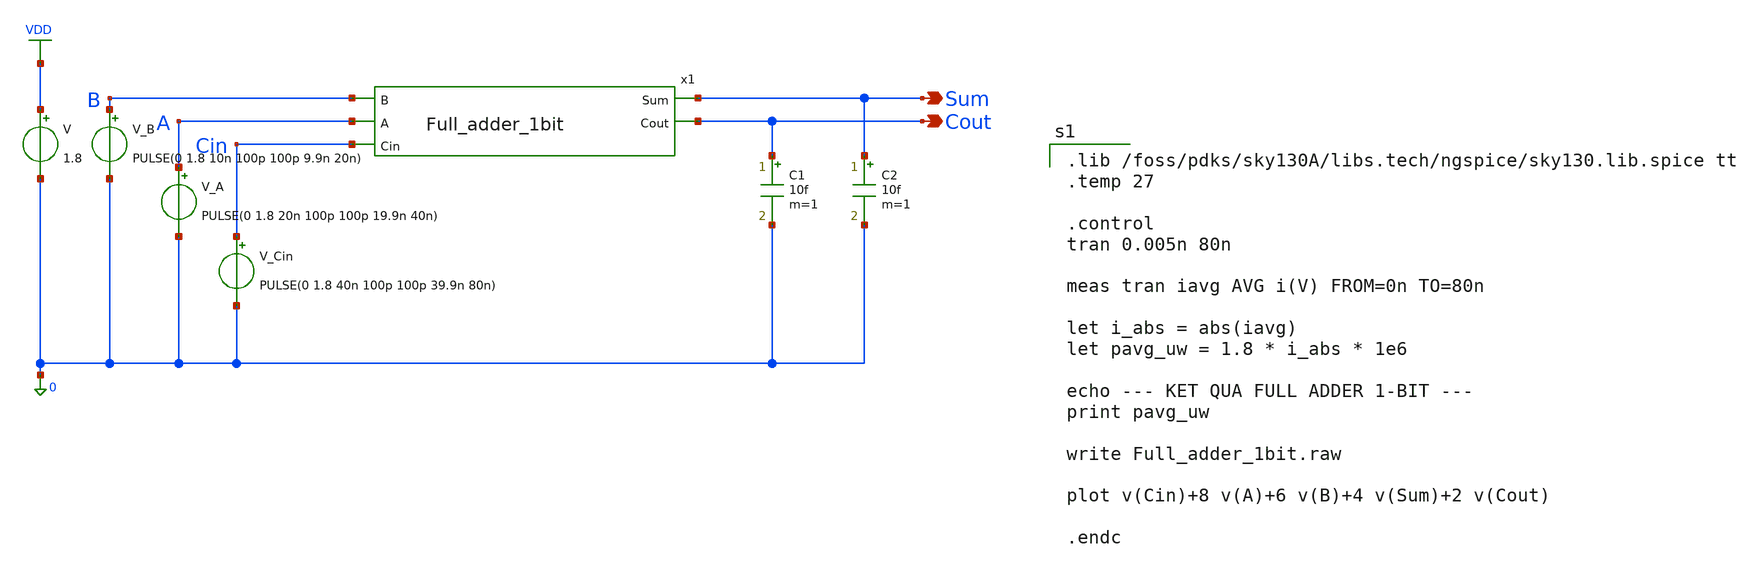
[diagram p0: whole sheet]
** sch_path: cells/full_adder_tg/xschem/tb_Full_adder_1bit.sch
**.subckt tb_Full_adder_1bit Sum Cout
*.opin Sum
*.opin Cout
x1 B A Sum Cin Cout Full_adder_1bit
V VDD 0 1.8
V_B B 0 PULSE(0 1.8 10n 100p 100p 9.9n 20n)
V_A A 0 PULSE(0 1.8 20n 100p 100p 19.9n 40n)
V_Cin Cin 0 PULSE(0 1.8 40n 100p 100p 39.9n 80n)
C1 Cout 0 10f m=1
C2 Sum 0 10f m=1
**.ends

* expanding   symbol:  ./Full_adder_1bit.sym # of pins=5
** sym_path: cells/full_adder_tg/xschem/Full_adder_1bit.sym
** sch_path: cells/full_adder_tg/xschem/Full_adder_1bit.sch
.subckt Full_adder_1bit B A Sum Cin Cout
*.ipin B
*.ipin A
*.ipin Cin
*.opin Sum
*.opin Cout
x1 A B P xor2_design_khaosat
x2 P Cin Sum xor2_design_khaosat
x3 Cin Cout P B mux_2to1_design
.ends


* expanding   symbol:  ./xor2_design_khaosat.sym # of pins=3
** sym_path: cells/full_adder_tg/xschem/xor2_design_khaosat.sym
** sch_path: cells/full_adder_tg/xschem/xor2_design_khaosat.sch
.subckt xor2_design_khaosat B A Y
*.opin Y
*.ipin B
*.ipin A
XMPmos_inv_1 net1 B VDD VDD sky130_fd_pr__pfet_01v8 L=0.15 W=5 nf=1 ad='int((1 + 1)/2) * 5 / 1 * 0.29'
+ as='int((1 + 2)/2) * 5 / 1 * 0.29' pd='2*int((1 + 1)/2) * (5 / 1 + 0.29)' ps='2*int((1 + 2)/2) * (5 / 1 + 0.29)'
+ nrd='0.29 / 5 ' nrs='0.29 / 5 ' sa=0 sb=0 sd=0 mult=1 m=1
XMNmos_inv_1 net1 B 0 0 sky130_fd_pr__nfet_01v8 L=0.15 W=2 nf=1 ad='int((1 + 1)/2) * 2 / 1 * 0.29' as='int((1 + 2)/2) * 2 / 1 * 0.29'
+ pd='2*int((1 + 1)/2) * (2 / 1 + 0.29)' ps='2*int((1 + 2)/2) * (2 / 1 + 0.29)' nrd='0.29 / 2 ' nrs='0.29 / 2 '
+ sa=0 sb=0 sd=0 mult=1 m=1
XMPmos_xor_1 Y B A VDD sky130_fd_pr__pfet_01v8 L=0.15 W=5 nf=1 ad='int((1 + 1)/2) * 5 / 1 * 0.29' as='int((1 + 2)/2) * 5 / 1 * 0.29'
+ pd='2*int((1 + 1)/2) * (5 / 1 + 0.29)' ps='2*int((1 + 2)/2) * (5 / 1 + 0.29)' nrd='0.29 / 5 ' nrs='0.29 / 5 '
+ sa=0 sb=0 sd=0 mult=1 m=1
XMNmos_xor_1 Y net1 A 0 sky130_fd_pr__nfet_01v8 L=0.15 W=2 nf=1 ad='int((1 + 1)/2) * 2 / 1 * 0.29' as='int((1 + 2)/2) * 2 / 1 * 0.29'
+ pd='2*int((1 + 1)/2) * (2 / 1 + 0.29)' ps='2*int((1 + 2)/2) * (2 / 1 + 0.29)' nrd='0.29 / 2 ' nrs='0.29 / 2 '
+ sa=0 sb=0 sd=0 mult=1 m=1
XMPmos_xor_2 Y A B VDD sky130_fd_pr__pfet_01v8 L=0.15 W=5 nf=1 ad='int((1 + 1)/2) * 5 / 1 * 0.29' as='int((1 + 2)/2) * 5 / 1 * 0.29'
+ pd='2*int((1 + 1)/2) * (5 / 1 + 0.29)' ps='2*int((1 + 2)/2) * (5 / 1 + 0.29)' nrd='0.29 / 5 ' nrs='0.29 / 5 '
+ sa=0 sb=0 sd=0 mult=1 m=1
XMNmos_xor_2 Y A net1 0 sky130_fd_pr__nfet_01v8 L=0.15 W=2 nf=1 ad='int((1 + 1)/2) * 2 / 1 * 0.29' as='int((1 + 2)/2) * 2 / 1 * 0.29'
+ pd='2*int((1 + 1)/2) * (2 / 1 + 0.29)' ps='2*int((1 + 2)/2) * (2 / 1 + 0.29)' nrd='0.29 / 2 ' nrs='0.29 / 2 '
+ sa=0 sb=0 sd=0 mult=1 m=1
.ends


* expanding   symbol:  ./mux_2to1_design.sym # of pins=4
** sym_path: cells/full_adder_tg/xschem/mux_2to1_design.sym
** sch_path: cells/full_adder_tg/xschem/mux_2to1_design.sch
.subckt mux_2to1_design Int_1 Y S Int_0
*.ipin Int_1
*.ipin Int_0
*.opin Y
*.ipin S
XMNmos_1 Y S Int_1 0 sky130_fd_pr__nfet_01v8 L=0.15 W=2 nf=1 ad='int((1 + 1)/2) * 2 / 1 * 0.29' as='int((1 + 2)/2) * 2 / 1 * 0.29'
+ pd='2*int((1 + 1)/2) * (2 / 1 + 0.29)' ps='2*int((1 + 2)/2) * (2 / 1 + 0.29)' nrd='0.29 / 2 ' nrs='0.29 / 2 '
+ sa=0 sb=0 sd=0 mult=1 m=1
XMPmos_1 Y net1 Int_1 VDD sky130_fd_pr__pfet_01v8 L=0.15 W=5 nf=1 ad='int((1 + 1)/2) * 5 / 1 * 0.29'
+ as='int((1 + 2)/2) * 5 / 1 * 0.29' pd='2*int((1 + 1)/2) * (5 / 1 + 0.29)' ps='2*int((1 + 2)/2) * (5 / 1 + 0.29)'
+ nrd='0.29 / 5 ' nrs='0.29 / 5 ' sa=0 sb=0 sd=0 mult=1 m=1
XMNmos_2 Y net1 Int_0 0 sky130_fd_pr__nfet_01v8 L=0.15 W=2 nf=1 ad='int((1 + 1)/2) * 2 / 1 * 0.29' as='int((1 + 2)/2) * 2 / 1 * 0.29'
+ pd='2*int((1 + 1)/2) * (2 / 1 + 0.29)' ps='2*int((1 + 2)/2) * (2 / 1 + 0.29)' nrd='0.29 / 2 ' nrs='0.29 / 2 '
+ sa=0 sb=0 sd=0 mult=1 m=1
XMPmos_2 Y S Int_0 VDD sky130_fd_pr__pfet_01v8 L=0.15 W=5 nf=1 ad='int((1 + 1)/2) * 5 / 1 * 0.29' as='int((1 + 2)/2) * 5 / 1 * 0.29'
+ pd='2*int((1 + 1)/2) * (5 / 1 + 0.29)' ps='2*int((1 + 2)/2) * (5 / 1 + 0.29)' nrd='0.29 / 5 ' nrs='0.29 / 5 '
+ sa=0 sb=0 sd=0 mult=1 m=1
x1 net1 S inveter_design
.ends


* expanding   symbol:  ./inveter_design.sym # of pins=2
** sym_path: cells/full_adder_tg/xschem/inveter_design.sym
** sch_path: cells/full_adder_tg/xschem/inveter_design.sch
.subckt inveter_design Out In
*.ipin In
*.opin Out
XMNMOS Out In 0 0 sky130_fd_pr__nfet_01v8 L=0.15 W=2 nf=1 ad='int((1 + 1)/2) * 2 / 1 * 0.29' as='int((1 + 2)/2) * 2 / 1 * 0.29'
+ pd='2*int((1 + 1)/2) * (2 / 1 + 0.29)' ps='2*int((1 + 2)/2) * (2 / 1 + 0.29)' nrd='0.29 / 2 ' nrs='0.29 / 2 '
+ sa=0 sb=0 sd=0 mult=1 m=1
XMPMOS Out In VDD VDD sky130_fd_pr__pfet_01v8 L=0.15 W=5 nf=1 ad='int((1 + 1)/2) * 5 / 1 * 0.29' as='int((1 + 2)/2) * 5 / 1 * 0.29'
+ pd='2*int((1 + 1)/2) * (5 / 1 + 0.29)' ps='2*int((1 + 2)/2) * (5 / 1 + 0.29)' nrd='0.29 / 5 ' nrs='0.29 / 5 '
+ sa=0 sb=0 sd=0 mult=1 m=1
.ends

.GLOBAL VDD
**** begin user architecture code

.lib /foss/pdks/sky130A/libs.tech/ngspice/sky130.lib.spice tt
.temp 27

.control
tran 0.005n 80n

meas tran iavg AVG i(V) FROM=0n TO=80n

let i_abs = abs(iavg)
let pavg_uw = 1.8 * i_abs * 1e6

echo --- KET QUA FULL ADDER 1-BIT ---
print pavg_uw

write Full_adder_1bit.raw

plot v(Cin)+8 v(A)+6 v(B)+4 v(Sum)+2 v(Cout)

.endc

**** end user architecture code
.end
